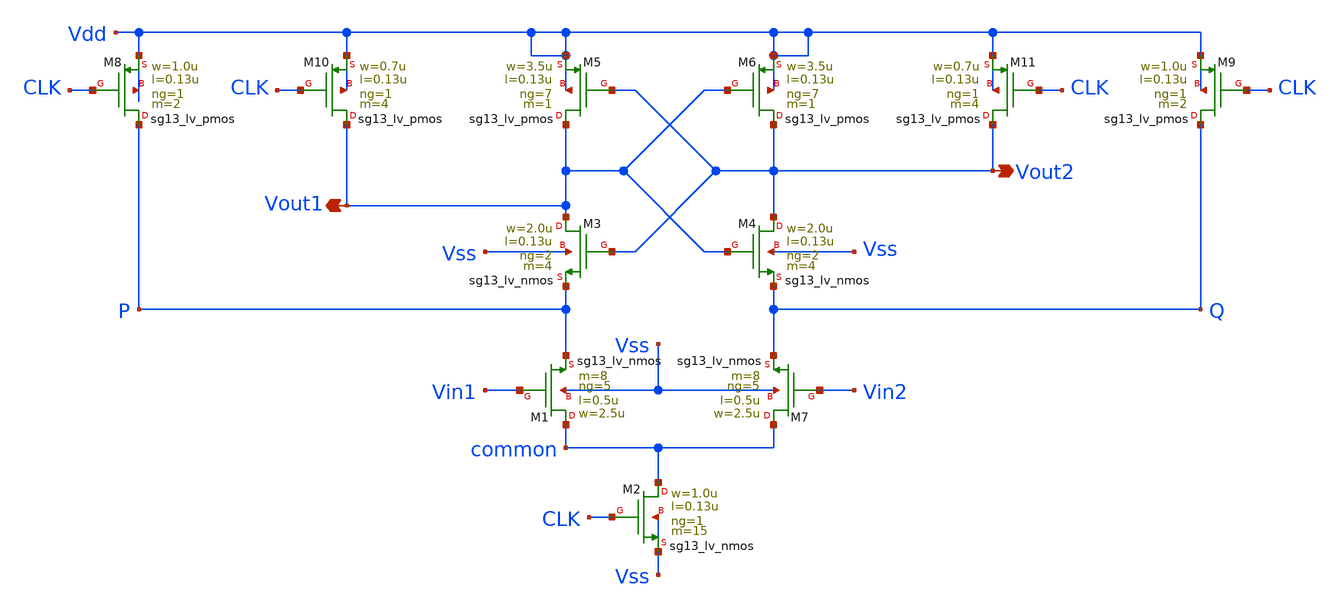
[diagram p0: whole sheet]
** sch_path: klayout/LVS/SA.sch
**.subckt SA Vout2 Vout1
*.opin Vout2
*.opin Vout1
XM4 Vout2 Vout1 Q Vss sg13_lv_nmos w=2.0u l=0.13u ng=2 m=4 mm_ok=1
XM6 Vout2 Vout1 Vdd Vdd sg13_lv_pmos w=3.5u l=0.13u ng=7 m=1 mm_ok=1
XM11 Vout2 CLK Vdd Vdd sg13_lv_pmos w=0.7u l=0.13u ng=1 m=4 mm_ok=1
XM9 Q CLK Vdd Vdd sg13_lv_pmos w=1.0u l=0.13u ng=1 m=2 mm_ok=1
XM3 Vout1 Vout2 P Vss sg13_lv_nmos w=2.0u l=0.13u ng=2 m=4 mm_ok=1
XM5 Vout1 Vout2 Vdd Vdd sg13_lv_pmos w=3.5u l=0.13u ng=7 m=1 mm_ok=1
XM10 Vout1 CLK Vdd Vdd sg13_lv_pmos w=0.7u l=0.13u ng=1 m=4 mm_ok=1
XM8 P CLK Vdd Vdd sg13_lv_pmos w=1.0u l=0.13u ng=1 m=2 mm_ok=1
XM1 common Vin1 P Vss sg13_lv_nmos w=2.5u l=0.5u ng=5 m=8 mm_ok=1
XM2 common CLK Vss Vss sg13_lv_nmos w=1.0u l=0.13u ng=1 m=15 mm_ok=1
XM7 common Vin2 Q Vss sg13_lv_nmos w=2.5u l=0.5u ng=5 m=8 mm_ok=1
**.ends
.end
